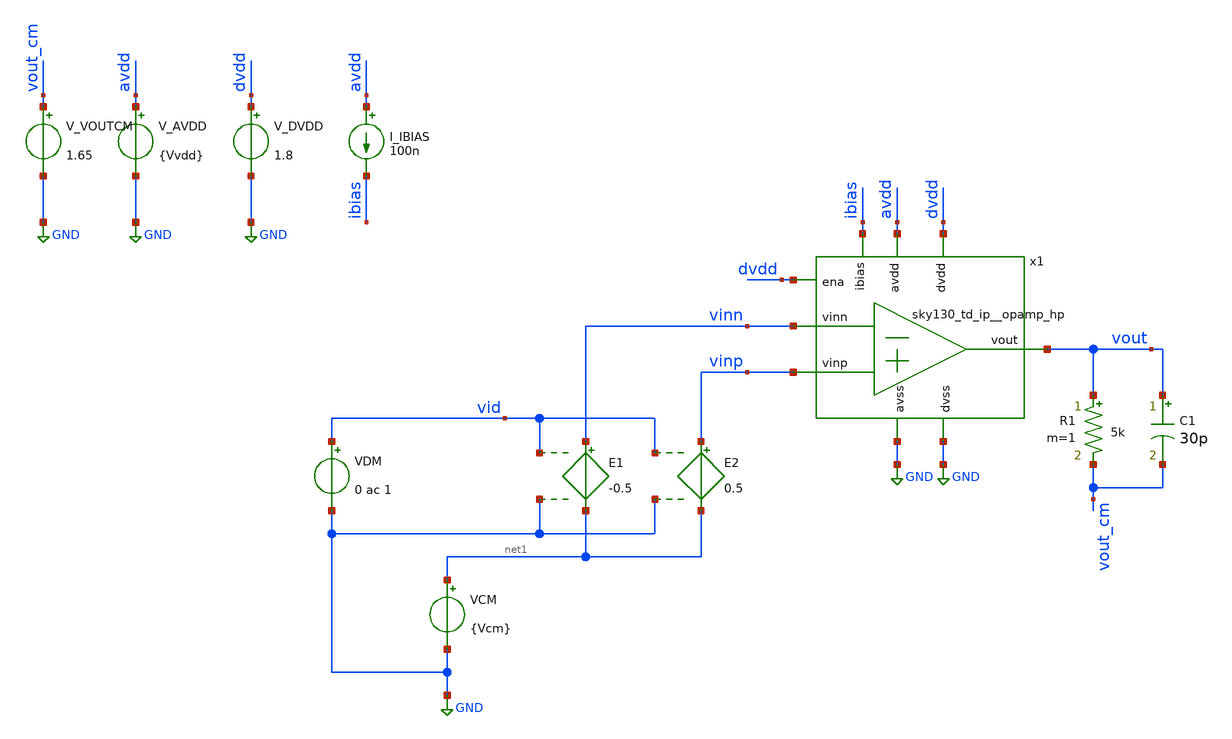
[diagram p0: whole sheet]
** sch_path: cace/input_offset.sch
**.subckt input_offset
x1 avdd vout ibias vinn vinp GND dvdd GND dvdd sky130_td_ip__opamp_hp
V_AVDD avdd GND {Vvdd}
.save i(v_avdd)
V_DVDD dvdd GND 1.8
.save i(v_dvdd)
I_IBIAS avdd ibias 100n
VCM net1 GND {Vcm}
R1 vout vout_cm 5k m=1
C1 vout vout_cm 30p m=1
V_VOUTCM vout_cm GND 1.65
.save i(v_voutcm)
E1 vinn net1 vid GND -0.5
VDM vid GND 0 ac 1
E2 vinp net1 vid GND 0.5
**** begin user architecture code


.save all

.control
save all
alter @VDM[pwl] = [ 0 -10m 10 10m ]
tran 1m 10
run
let vid = v(vid)
let vout = v(vout)
meas tran input_offset_voltage FIND vid WHEN vout=1.65 RISE=LAST

echo
echo ===================================
echo Differential-mode DC sweep results
echo - Input Offset voltage: $&input_offset_voltage
echo ===================================

echo $&input_offset_voltage > {simpath}/{filename}_{N}.data

*plot vout

quit

.endc




* CACE gensim simulation file {filename}_{N}
* Generated by CACE gensim, Efabless Corporation (c) 2023
* Find the power supply rejection ratio of the amplifier

.include {DUT_path}

.lib {PDK_ROOT}/{PDK}/libs.tech/combined/sky130.lib.spice {corner}

.option TEMP={temperature}
* Flag unsafe operating conditions (exceeds models' specified limits)
.option warn=1


**** end user architecture code
**.ends
.GLOBAL GND
.end
